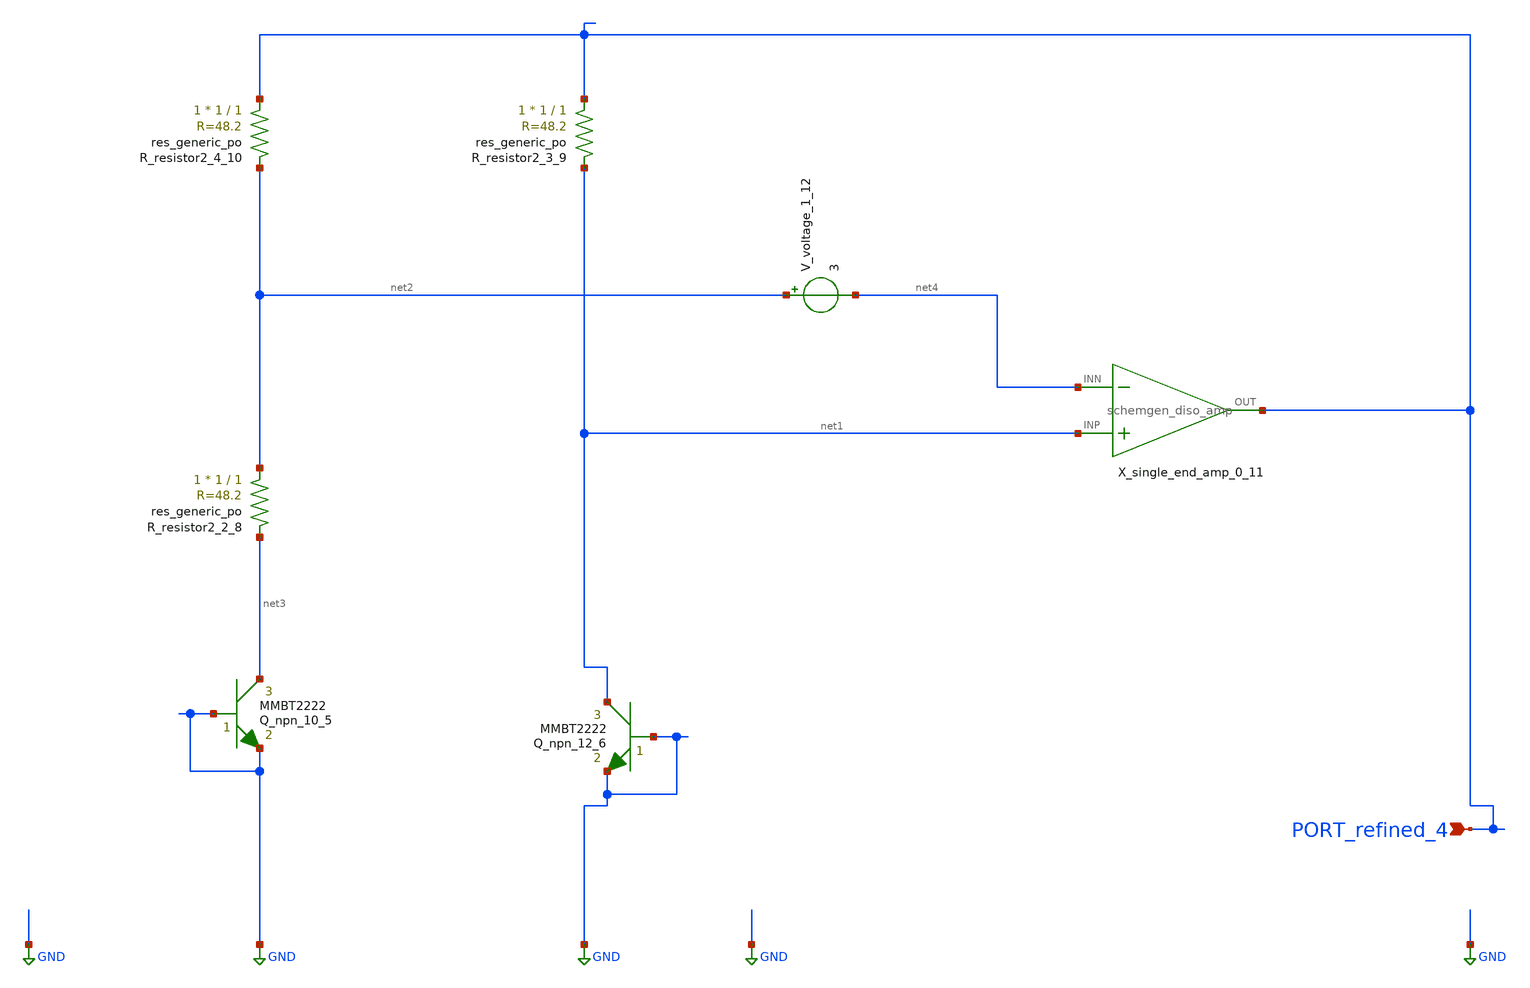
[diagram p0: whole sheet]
** sch_path: schematics/Image2Net/069.sch
**.subckt 069 PORT_refined_4
*.ipin PORT_refined_4
Q_npn_10_5 net3 GND GND MMBT2222 area=1 m=1
Q_npn_12_6 net1 GND GND MMBT2222 area=1 m=1
XR_resistor2_2_8 net2 net3 sky130_fd_pr__res_generic_po W=1 L=1 m=1
XR_resistor2_3_9 PORT_refined_4 net1 sky130_fd_pr__res_generic_po W=1 L=1 m=1
XR_resistor2_4_10 PORT_refined_4 net2 sky130_fd_pr__res_generic_po W=1 L=1 m=1
X_single_end_amp_0_11 net1 net4 PORT_refined_4 schemgen_diso_amp
V_voltage_1_12 net2 net4 3
**.ends

* expanding   symbol:  schemgen_diso_amp.sym # of pins=3
** sym_path: symbols/schemgen_diso_amp.sym
.subckt schemgen_diso_amp INP INN OUT
* SchemGen ideal op-amp: Vout = 1e5 * (V(INP) - V(INN))
E1 OUT 0 INP INN 1e5
.ends schemgen_diso_amp
.GLOBAL GND
.end
